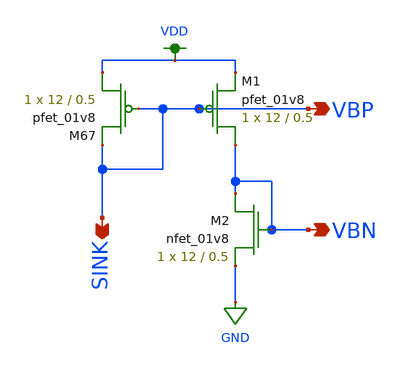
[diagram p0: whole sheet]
** sch_path: schemas/FCDA_BIAS.sch
**.subckt FCDA_BIAS VBP VBN SINK
*.opin VBP
*.opin VBN
*.opin SINK
XM67 VDD VBP VBP VDD sky130_fd_pr__pfet_01v8 L=0.5 W=12 nf=1 ad='int((nf+1)/2) * W/nf * 0.29' as='int((nf+2)/2) * W/nf * 0.29'
+ pd='2*int((nf+1)/2) * (W/nf + 0.29)' ps='2*int((nf+2)/2) * (W/nf + 0.29)' nrd='0.29 / W' nrs='0.29 / W'
+ sa=0 sb=0 sd=0 mult=1 m=1
XM1 VBN VBP VDD VDD sky130_fd_pr__pfet_01v8 L=0.5 W=12 nf=1 ad='int((nf+1)/2) * W/nf * 0.29' as='int((nf+2)/2) * W/nf * 0.29'
+ pd='2*int((nf+1)/2) * (W/nf + 0.29)' ps='2*int((nf+2)/2) * (W/nf + 0.29)' nrd='0.29 / W' nrs='0.29 / W'
+ sa=0 sb=0 sd=0 mult=1 m=1
XM2 VBN VBN GND GND sky130_fd_pr__nfet_01v8 L=0.5 W=12 nf=1 ad='int((nf+1)/2) * W/nf * 0.29' as='int((nf+2)/2) * W/nf * 0.29'
+ pd='2*int((nf+1)/2) * (W/nf + 0.29)' ps='2*int((nf+2)/2) * (W/nf + 0.29)' nrd='0.29 / W' nrs='0.29 / W'
+ sa=0 sb=0 sd=0 mult=1 m=1
**.ends
.GLOBAL VDD
.GLOBAL GND
.end
